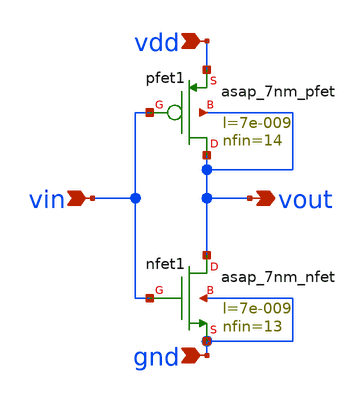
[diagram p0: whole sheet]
** sch_path: Xschem_ASAP7/inverter.sch
**.subckt inverter vin vdd gnd vout
*.ipin vin
*.ipin vdd
*.ipin gnd
*.opin vout
Xnfet1 vout vin gnd gnd asap_7nm_nfet l=7e-009 nfin=13
Xpfet1 vout vin vdd vout asap_7nm_pfet l=7e-009 nfin=14
**.ends
.end
